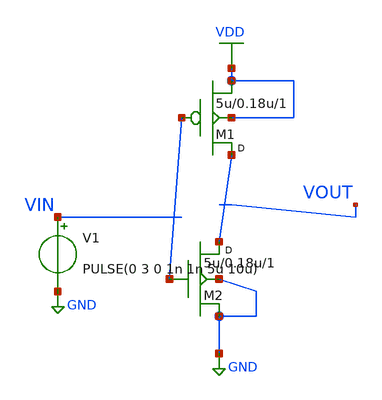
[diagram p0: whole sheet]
** sch_path: week3/day15/cmos schematic .sch
**.subckt cmos schematic
M1 net2 net1 VDD VDD pmos w=5u l=0.18u m=1
M2 net2 net1 GND GND nmos w=5u l=0.18u m=1
V1 VIN GND PULSE(0 3 0 1n 1n 5u 10u)
**** begin user architecture code
VIN
**** end user architecture code
**.ends
.GLOBAL VDD
.GLOBAL GND
.end
